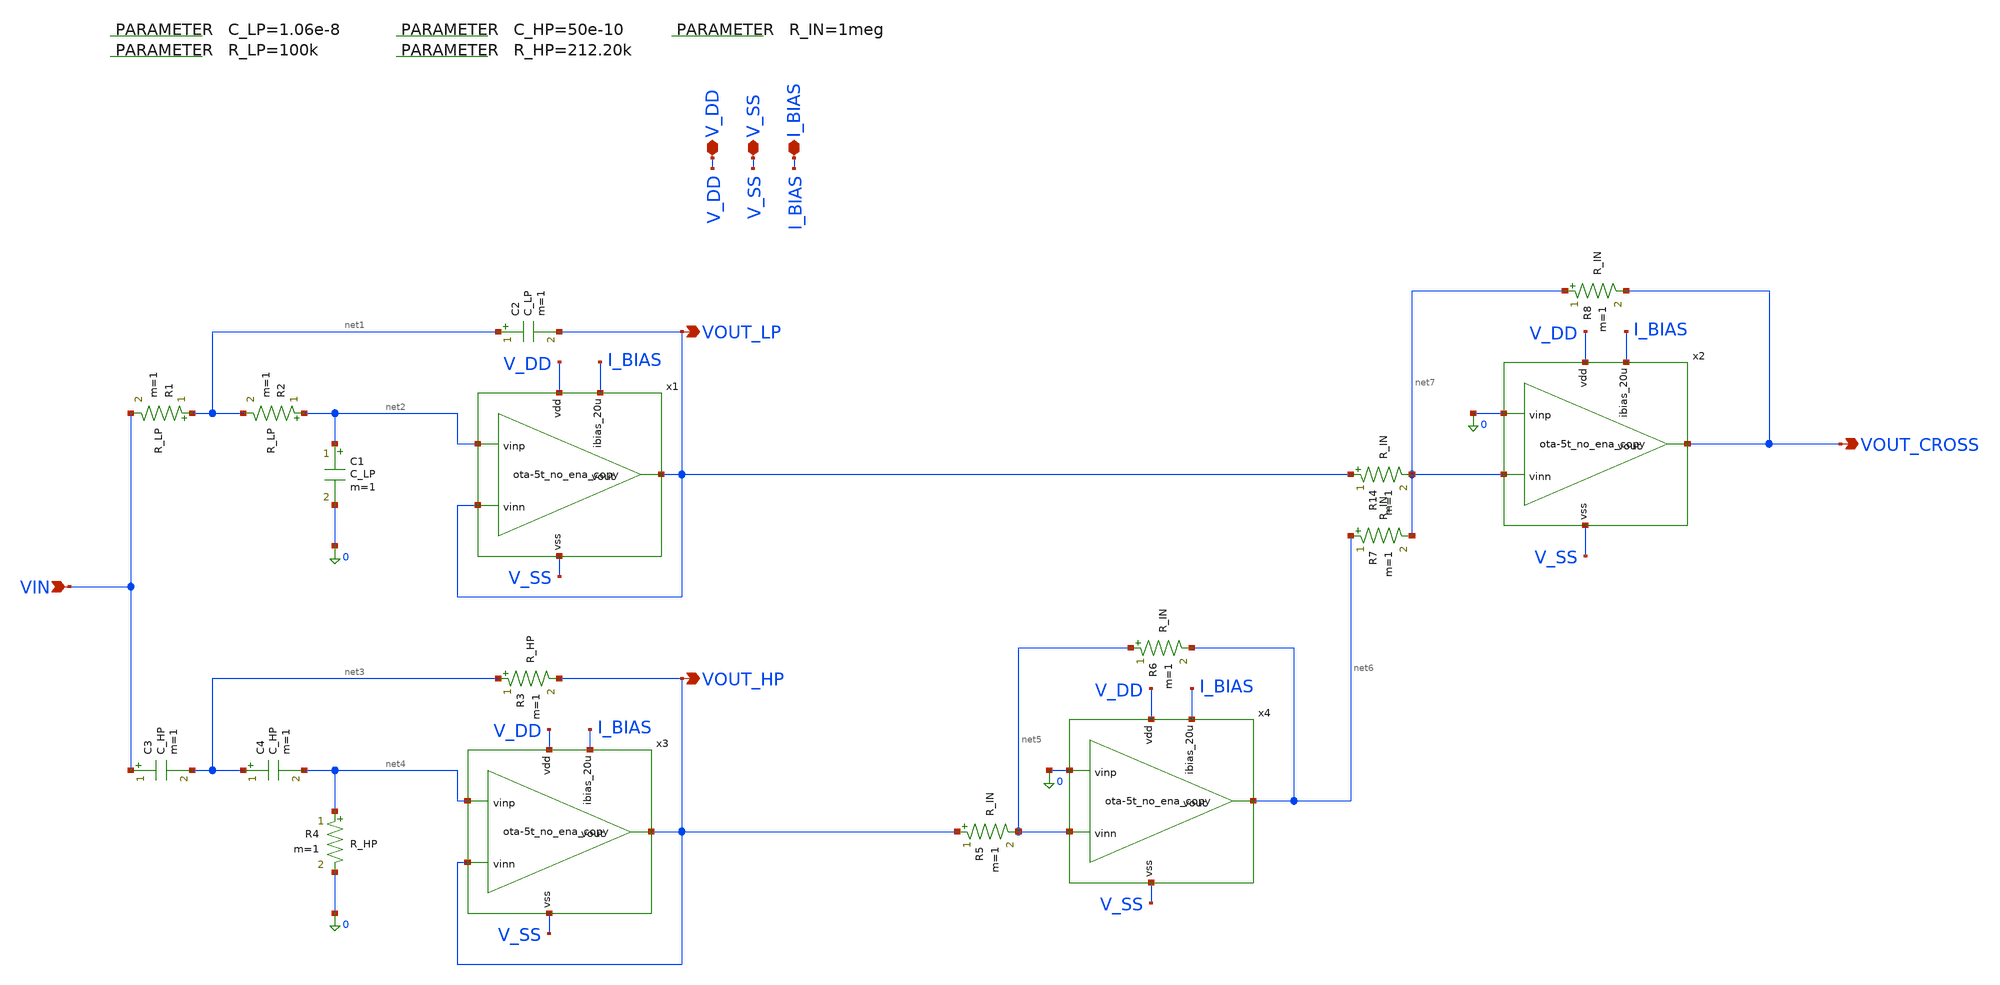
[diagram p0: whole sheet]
** sch_path: 004_Real_Circuits/002_version_no_enable/linkwtz_riley_crossover_pretl_OTA.sch
**.subckt linkwtz_riley_crossover_pretl_OTA VOUT_LP VIN V_DD VOUT_HP V_SS I_BIAS VOUT_CROSS
*.opin VOUT_LP
*.ipin VIN
*.iopin V_DD
*.opin VOUT_HP
*.iopin V_SS
*.iopin I_BIAS
*.opin VOUT_CROSS
R1 net1 VIN R_LP m=1
.param C_LP=1.06e-8
.param R_LP=100k
.param C_HP=50e-10
.param R_HP=212.20k
.param R_IN=1meg
R2 net2 net1 R_LP m=1
C1 net2 0 C_LP m=1
C2 net1 VOUT_LP C_LP m=1
C3 VIN net3 C_HP m=1
C4 net3 net4 C_HP m=1
R3 net3 VOUT_HP R_HP m=1
R4 net4 0 R_HP m=1
R5 VOUT_HP net5 R_IN m=1
R6 net5 net6 R_IN m=1
R14 VOUT_LP net7 R_IN m=1
R7 net6 net7 R_IN m=1
R8 net7 VOUT_CROSS R_IN m=1
x1 V_DD VOUT_LP net2 VOUT_LP I_BIAS V_SS ota-5t_no_ena_copy
x2 V_DD VOUT_CROSS 0 net7 I_BIAS V_SS ota-5t_no_ena_copy
x3 V_DD VOUT_HP net4 VOUT_HP I_BIAS V_SS ota-5t_no_ena_copy
x4 V_DD net6 0 net5 I_BIAS V_SS ota-5t_no_ena_copy
**.ends
.end
